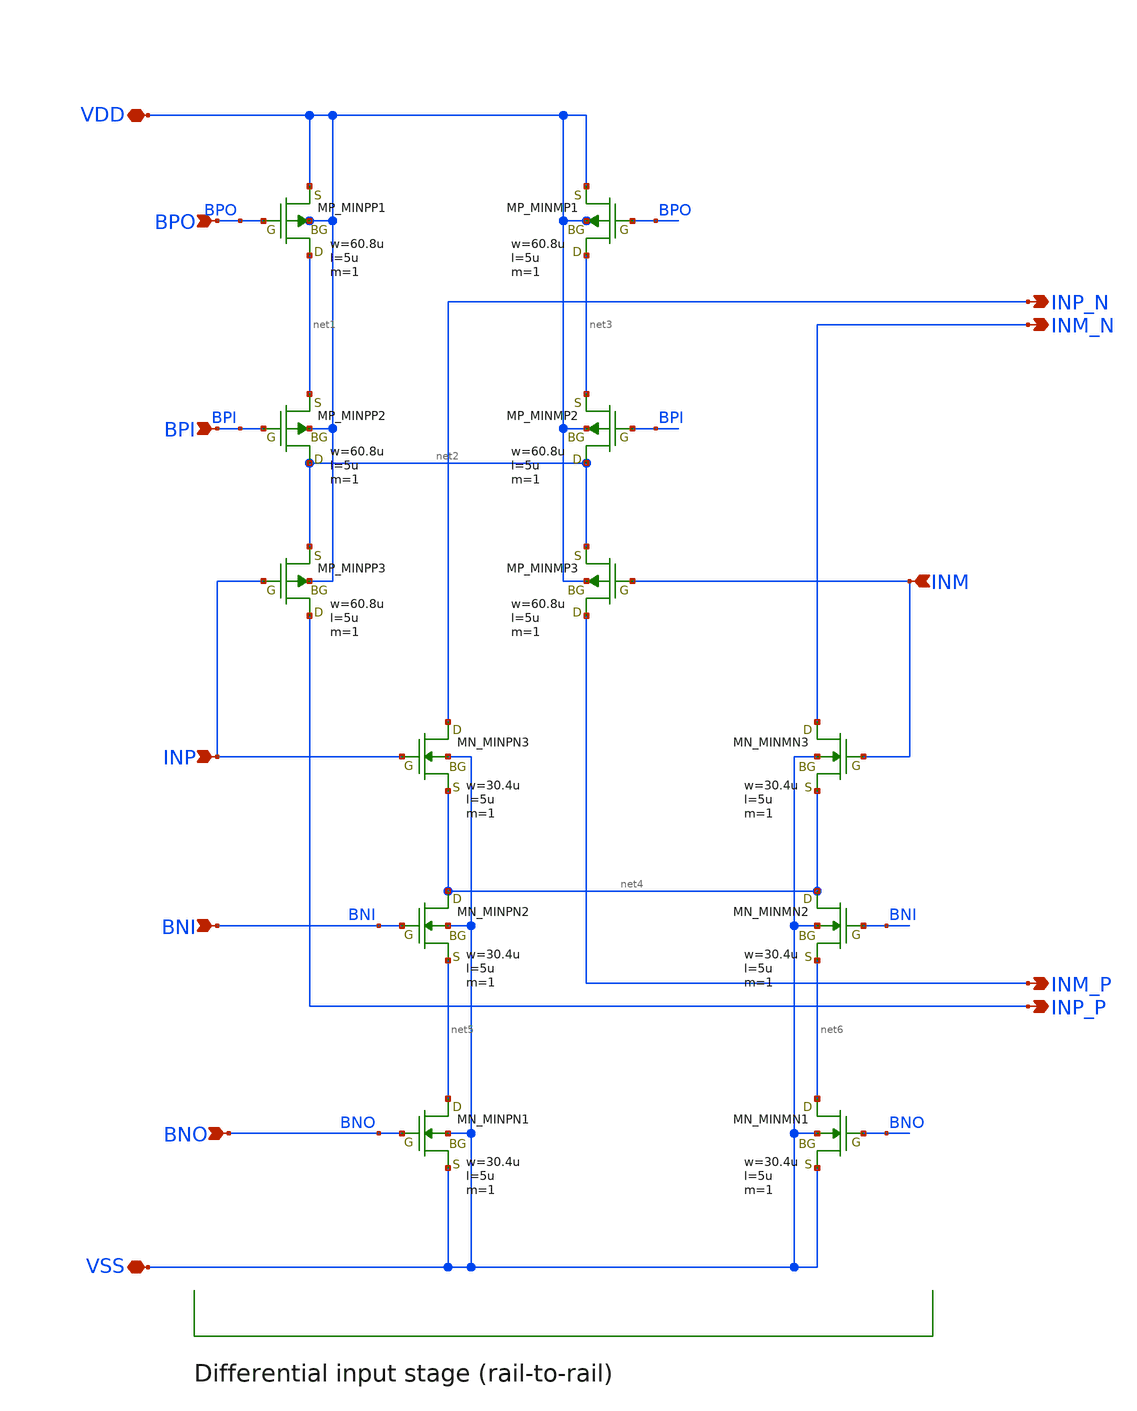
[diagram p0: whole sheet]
** sch_path: opamp_r2r_audio/MiyabiYoshino/opamp_r2r_diff_YoshinoMiyabi.sch
**.subckt opamp_r2r_diff_YoshinoMiyabi VDD VSS INP INM INP_N INM_N INM_P INP_P BPO BPI BNI BNO
*.iopin VDD
*.iopin VSS
*.ipin INP
*.ipin INM
*.opin INP_N
*.opin INM_N
*.opin INM_P
*.opin INP_P
*.ipin BPO
*.ipin BPI
*.ipin BNI
*.ipin BNO
XMINPP1 net1 BPO VDD VDD PMOS w=60.8u l=5u as=0 ad=0 ps=0 pd=0 nrd=0 nrs=0 m=1
XMINPP2 net2 BPI net1 VDD PMOS w=60.8u l=5u as=0 ad=0 ps=0 pd=0 nrd=0 nrs=0 m=1
XMINPP3 INP_P INP net2 VDD PMOS w=60.8u l=5u as=0 ad=0 ps=0 pd=0 nrd=0 nrs=0 m=1
XMINMP1 net3 BPO VDD VDD PMOS w=60.8u l=5u as=0 ad=0 ps=0 pd=0 nrd=0 nrs=0 m=1
XMINMP2 net2 BPI net3 VDD PMOS w=60.8u l=5u as=0 ad=0 ps=0 pd=0 nrd=0 nrs=0 m=1
XMINMP3 INM_P INM net2 VDD PMOS w=60.8u l=5u as=0 ad=0 ps=0 pd=0 nrd=0 nrs=0 m=1
XMINPN2 net4 BNI net5 VSS NMOS w=30.4u l=5u as=0 ad=0 ps=0 pd=0 nrd=0 nrs=0 m=1
XMINPN1 net5 BNO VSS VSS NMOS w=30.4u l=5u as=0 ad=0 ps=0 pd=0 nrd=0 nrs=0 m=1
XMINPN3 INP_N INP net4 VSS NMOS w=30.4u l=5u as=0 ad=0 ps=0 pd=0 nrd=0 nrs=0 m=1
XMINMN2 net4 BNI net6 VSS NMOS w=30.4u l=5u as=0 ad=0 ps=0 pd=0 nrd=0 nrs=0 m=1
XMINMN1 net6 BNO VSS VSS NMOS w=30.4u l=5u as=0 ad=0 ps=0 pd=0 nrd=0 nrs=0 m=1
XMINMN3 INM_N INM net4 VSS NMOS w=30.4u l=5u as=0 ad=0 ps=0 pd=0 nrd=0 nrs=0 m=1
**.ends
.end
